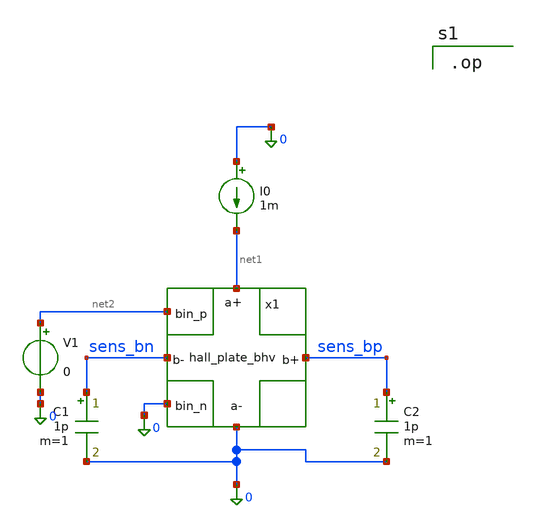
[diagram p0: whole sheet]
** sch_path: xschem/archive/hall_plate_bhv/hall_plate_bhv_tb.sch
**.subckt hall_plate_bhv_tb
I0 0 net1 1m
C2 sens_bp 0 1p m=1
x1 net1 sens_bp 0 sens_bn net2 0 hall_plate_bhv
C1 sens_bn 0 1p m=1
V1 net2 0 0
**** begin user architecture code

.op

**** end user architecture code
**.ends

* expanding   symbol:  hall_plate_bhv/hall_plate_bhv.sym # of pins=6
** sym_path: xschem/archive/hall_plate_bhv/hall_plate_bhv.sym
** sch_path: xschem/archive/hall_plate_bhv/hall_plate_bhv.sch
.subckt hall_plate_bhv sens_ap sens_bp sens_an sens_bn bin_p bin_n
*.iopin sens_bn
*.iopin sens_an
*.iopin sens_bp
*.iopin sens_ap
*.iopin bin_p
*.iopin bin_n
R1 net1 net2 {rh-0.5*roffset} m=1
R2 net1 net4 {rh} m=1
R3 net2 net3 {rh} m=1
R4 net4 net3 {rh-0.5*roffset} m=1
R5 net9 net2 {rd} m=1
B1 sens_bn net5 V = 0.5*i(Vap)*{sens_i}*(v(bin_p) - v(bin_n))
B2 sens_ap net6 V = 0.5*i(Vbp)*{sens_i}*(v(bin_p) - v(bin_n))
B3 sens_an net8 V = 0.5*i(Vbn)*{sens_i}*(v(bin_p) - v(bin_n))
B4 sens_bp net7 V = 0.5*i(Van)*{sens_i}*(v(bin_p) - v(bin_n))
Vbn net5 net2 0
Vap net6 net1 0
Vbp net7 net4 0
Van net8 net3 0
R6 net9 net1 {rd} m=1
R7 net9 net3 {rd} m=1
R8 net4 net9 {rd} m=1
**** begin user architecture code

.param nw_rsheet = 1000
.param device_l = 25u
.param device_w = 25u
.param r_mismatch = 0.05
.param nw_mu = 0.1
.param hall_factor = 1
.param pi = acos(-1)
.param qnt = 1/(nw_mu*nw_rsheet)
.param g = 1 - 5.0267*exp(-(pi/2)*(device_w+2*device_l)/device_w)
.param rh = (2*nw_rsheet/pi) * ((2*(device_l/device_w) + 2/3)*pi - 2*ln(2))
.param rh_rd_ratio = 2 - (8/pi) * (ln(2) / (2*(device_l/device_w) + 2/3))
.param rd = rh/rh_rd_ratio
.param roffset = r_mismatch*rh
.param sens_i = (g*hall_factor)/qnt

**** end user architecture code
.ends

.end
